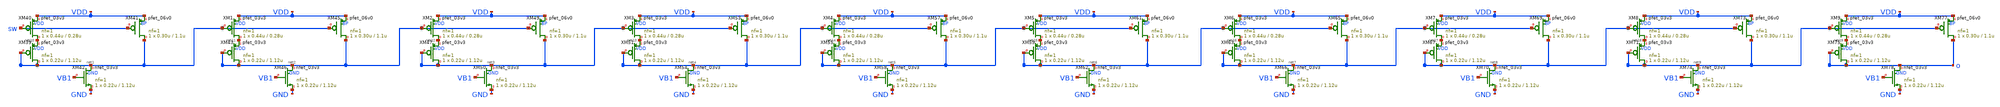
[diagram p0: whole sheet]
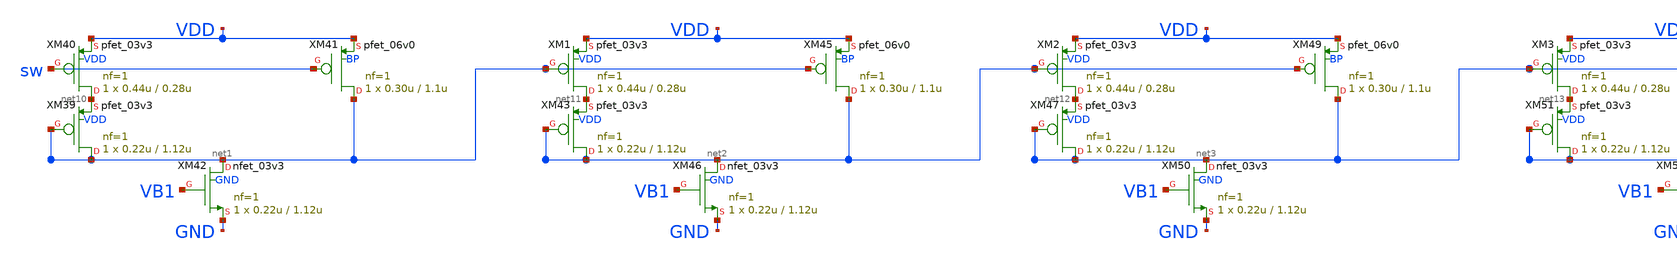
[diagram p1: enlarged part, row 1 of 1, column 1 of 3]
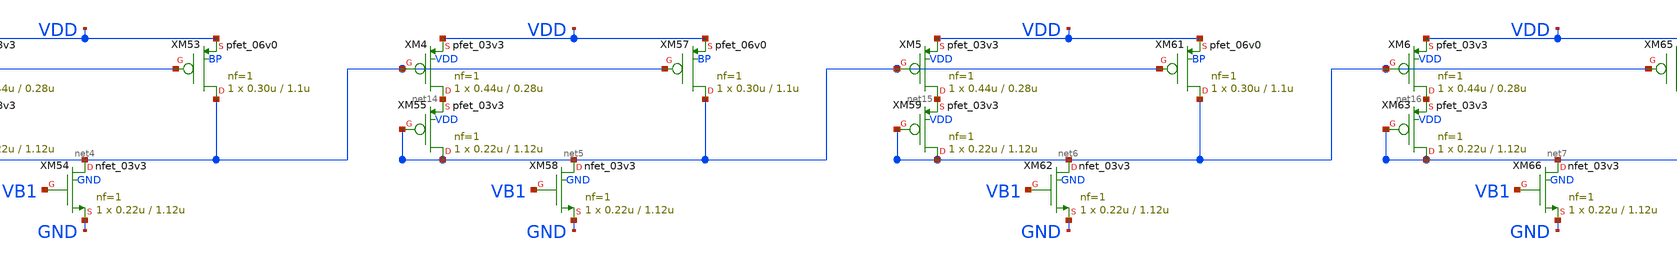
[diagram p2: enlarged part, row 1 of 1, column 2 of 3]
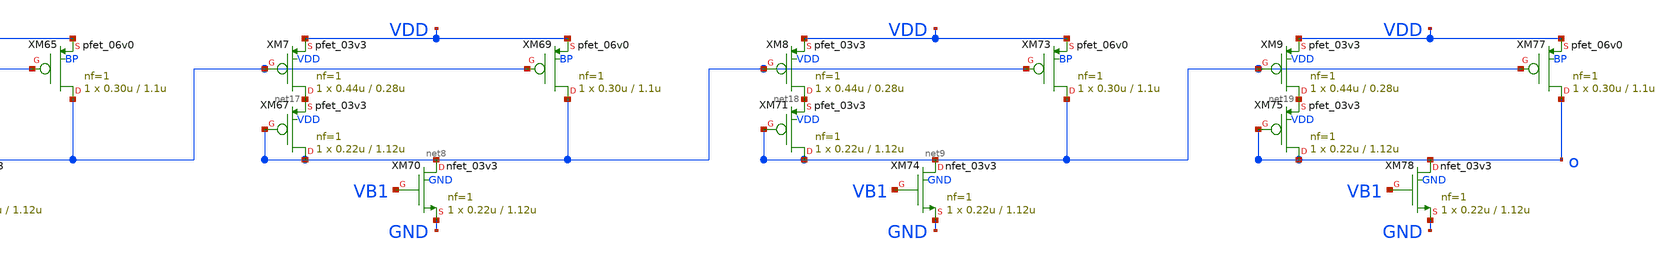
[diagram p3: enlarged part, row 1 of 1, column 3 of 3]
** sch_path: xschem_designs/STI_P_MC_TB.sch
**.subckt STI_P_MC_TB
XM39 net1 net1 net10 VDD pfet_03v3 L=1.12u W=0.22u nf=1 ad='int((nf+1)/2) * W/nf * 0.18u' as='int((nf+2)/2) * W/nf * 0.18u'
+ pd='2*int((nf+1)/2) * (W/nf + 0.18u)' ps='2*int((nf+2)/2) * (W/nf + 0.18u)' nrd='0.18u / W' nrs='0.18u / W'
+ sa=0 sb=0 sd=0 m=1 par=1
XM42 net1 VB1 GND GND nfet_03v3 L=1.12u W=0.22u nf=1 ad='int((nf+1)/2) * W/nf * 0.18u' as='int((nf+2)/2) * W/nf * 0.18u'
+ pd='2*int((nf+1)/2) * (W/nf + 0.18u)' ps='2*int((nf+2)/2) * (W/nf + 0.18u)' nrd='0.18u / W' nrs='0.18u / W'
+ sa=0 sb=0 sd=0 m=1 par=1
XM43 net2 net2 net11 VDD pfet_03v3 L=1.12u W=0.22u nf=1 ad='int((nf+1)/2) * W/nf * 0.18u' as='int((nf+2)/2) * W/nf * 0.18u'
+ pd='2*int((nf+1)/2) * (W/nf + 0.18u)' ps='2*int((nf+2)/2) * (W/nf + 0.18u)' nrd='0.18u / W' nrs='0.18u / W'
+ sa=0 sb=0 sd=0 m=1 par=1
XM46 net2 VB1 GND GND nfet_03v3 L=1.12u W=0.22u nf=1 ad='int((nf+1)/2) * W/nf * 0.18u' as='int((nf+2)/2) * W/nf * 0.18u'
+ pd='2*int((nf+1)/2) * (W/nf + 0.18u)' ps='2*int((nf+2)/2) * (W/nf + 0.18u)' nrd='0.18u / W' nrs='0.18u / W'
+ sa=0 sb=0 sd=0 m=1 par=1
XM47 net3 net3 net12 VDD pfet_03v3 L=1.12u W=0.22u nf=1 ad='int((nf+1)/2) * W/nf * 0.18u' as='int((nf+2)/2) * W/nf * 0.18u'
+ pd='2*int((nf+1)/2) * (W/nf + 0.18u)' ps='2*int((nf+2)/2) * (W/nf + 0.18u)' nrd='0.18u / W' nrs='0.18u / W'
+ sa=0 sb=0 sd=0 m=1 par=1
XM50 net3 VB1 GND GND nfet_03v3 L=1.12u W=0.22u nf=1 ad='int((nf+1)/2) * W/nf * 0.18u' as='int((nf+2)/2) * W/nf * 0.18u'
+ pd='2*int((nf+1)/2) * (W/nf + 0.18u)' ps='2*int((nf+2)/2) * (W/nf + 0.18u)' nrd='0.18u / W' nrs='0.18u / W'
+ sa=0 sb=0 sd=0 m=1 par=1
XM51 net4 net4 net13 VDD pfet_03v3 L=1.12u W=0.22u nf=1 ad='int((nf+1)/2) * W/nf * 0.18u' as='int((nf+2)/2) * W/nf * 0.18u'
+ pd='2*int((nf+1)/2) * (W/nf + 0.18u)' ps='2*int((nf+2)/2) * (W/nf + 0.18u)' nrd='0.18u / W' nrs='0.18u / W'
+ sa=0 sb=0 sd=0 m=1 par=1
XM54 net4 VB1 GND GND nfet_03v3 L=1.12u W=0.22u nf=1 ad='int((nf+1)/2) * W/nf * 0.18u' as='int((nf+2)/2) * W/nf * 0.18u'
+ pd='2*int((nf+1)/2) * (W/nf + 0.18u)' ps='2*int((nf+2)/2) * (W/nf + 0.18u)' nrd='0.18u / W' nrs='0.18u / W'
+ sa=0 sb=0 sd=0 m=1 par=1
XM55 net5 net5 net14 VDD pfet_03v3 L=1.12u W=0.22u nf=1 ad='int((nf+1)/2) * W/nf * 0.18u' as='int((nf+2)/2) * W/nf * 0.18u'
+ pd='2*int((nf+1)/2) * (W/nf + 0.18u)' ps='2*int((nf+2)/2) * (W/nf + 0.18u)' nrd='0.18u / W' nrs='0.18u / W'
+ sa=0 sb=0 sd=0 m=1 par=1
XM58 net5 VB1 GND GND nfet_03v3 L=1.12u W=0.22u nf=1 ad='int((nf+1)/2) * W/nf * 0.18u' as='int((nf+2)/2) * W/nf * 0.18u'
+ pd='2*int((nf+1)/2) * (W/nf + 0.18u)' ps='2*int((nf+2)/2) * (W/nf + 0.18u)' nrd='0.18u / W' nrs='0.18u / W'
+ sa=0 sb=0 sd=0 m=1 par=1
XM59 net6 net6 net15 VDD pfet_03v3 L=1.12u W=0.22u nf=1 ad='int((nf+1)/2) * W/nf * 0.18u' as='int((nf+2)/2) * W/nf * 0.18u'
+ pd='2*int((nf+1)/2) * (W/nf + 0.18u)' ps='2*int((nf+2)/2) * (W/nf + 0.18u)' nrd='0.18u / W' nrs='0.18u / W'
+ sa=0 sb=0 sd=0 m=1 par=1
XM62 net6 VB1 GND GND nfet_03v3 L=1.12u W=0.22u nf=1 ad='int((nf+1)/2) * W/nf * 0.18u' as='int((nf+2)/2) * W/nf * 0.18u'
+ pd='2*int((nf+1)/2) * (W/nf + 0.18u)' ps='2*int((nf+2)/2) * (W/nf + 0.18u)' nrd='0.18u / W' nrs='0.18u / W'
+ sa=0 sb=0 sd=0 m=1 par=1
XM63 net7 net7 net16 VDD pfet_03v3 L=1.12u W=0.22u nf=1 ad='int((nf+1)/2) * W/nf * 0.18u' as='int((nf+2)/2) * W/nf * 0.18u'
+ pd='2*int((nf+1)/2) * (W/nf + 0.18u)' ps='2*int((nf+2)/2) * (W/nf + 0.18u)' nrd='0.18u / W' nrs='0.18u / W'
+ sa=0 sb=0 sd=0 m=1 par=1
XM66 net7 VB1 GND GND nfet_03v3 L=1.12u W=0.22u nf=1 ad='int((nf+1)/2) * W/nf * 0.18u' as='int((nf+2)/2) * W/nf * 0.18u'
+ pd='2*int((nf+1)/2) * (W/nf + 0.18u)' ps='2*int((nf+2)/2) * (W/nf + 0.18u)' nrd='0.18u / W' nrs='0.18u / W'
+ sa=0 sb=0 sd=0 m=1 par=1
XM67 net8 net8 net17 VDD pfet_03v3 L=1.12u W=0.22u nf=1 ad='int((nf+1)/2) * W/nf * 0.18u' as='int((nf+2)/2) * W/nf * 0.18u'
+ pd='2*int((nf+1)/2) * (W/nf + 0.18u)' ps='2*int((nf+2)/2) * (W/nf + 0.18u)' nrd='0.18u / W' nrs='0.18u / W'
+ sa=0 sb=0 sd=0 m=1 par=1
XM70 net8 VB1 GND GND nfet_03v3 L=1.12u W=0.22u nf=1 ad='int((nf+1)/2) * W/nf * 0.18u' as='int((nf+2)/2) * W/nf * 0.18u'
+ pd='2*int((nf+1)/2) * (W/nf + 0.18u)' ps='2*int((nf+2)/2) * (W/nf + 0.18u)' nrd='0.18u / W' nrs='0.18u / W'
+ sa=0 sb=0 sd=0 m=1 par=1
XM71 net9 net9 net18 VDD pfet_03v3 L=1.12u W=0.22u nf=1 ad='int((nf+1)/2) * W/nf * 0.18u' as='int((nf+2)/2) * W/nf * 0.18u'
+ pd='2*int((nf+1)/2) * (W/nf + 0.18u)' ps='2*int((nf+2)/2) * (W/nf + 0.18u)' nrd='0.18u / W' nrs='0.18u / W'
+ sa=0 sb=0 sd=0 m=1 par=1
XM74 net9 VB1 GND GND nfet_03v3 L=1.12u W=0.22u nf=1 ad='int((nf+1)/2) * W/nf * 0.18u' as='int((nf+2)/2) * W/nf * 0.18u'
+ pd='2*int((nf+1)/2) * (W/nf + 0.18u)' ps='2*int((nf+2)/2) * (W/nf + 0.18u)' nrd='0.18u / W' nrs='0.18u / W'
+ sa=0 sb=0 sd=0 m=1 par=1
XM75 o o net19 VDD pfet_03v3 L=1.12u W=0.22u nf=1 ad='int((nf+1)/2) * W/nf * 0.18u' as='int((nf+2)/2) * W/nf * 0.18u'
+ pd='2*int((nf+1)/2) * (W/nf + 0.18u)' ps='2*int((nf+2)/2) * (W/nf + 0.18u)' nrd='0.18u / W' nrs='0.18u / W'
+ sa=0 sb=0 sd=0 m=1 par=1
XM78 o VB1 GND GND nfet_03v3 L=1.12u W=0.22u nf=1 ad='int((nf+1)/2) * W/nf * 0.18u' as='int((nf+2)/2) * W/nf * 0.18u'
+ pd='2*int((nf+1)/2) * (W/nf + 0.18u)' ps='2*int((nf+2)/2) * (W/nf + 0.18u)' nrd='0.18u / W' nrs='0.18u / W'
+ sa=0 sb=0 sd=0 m=1 par=1
XM41 net1 sw VDD BP pfet_06v0 L=1.1u W=0.30u nf=1 ad='int((nf+1)/2) * W/nf * 0.18u' as='int((nf+2)/2) * W/nf * 0.18u'
+ pd='2*int((nf+1)/2) * (W/nf + 0.18u)' ps='2*int((nf+2)/2) * (W/nf + 0.18u)' nrd='0.18u / W' nrs='0.18u / W'
+ sa=0 sb=0 sd=0 m=1 par=1
XM45 net2 net1 VDD BP pfet_06v0 L=1.1u W=0.30u nf=1 ad='int((nf+1)/2) * W/nf * 0.18u' as='int((nf+2)/2) * W/nf * 0.18u'
+ pd='2*int((nf+1)/2) * (W/nf + 0.18u)' ps='2*int((nf+2)/2) * (W/nf + 0.18u)' nrd='0.18u / W' nrs='0.18u / W'
+ sa=0 sb=0 sd=0 m=1 par=1
XM49 net3 net2 VDD BP pfet_06v0 L=1.1u W=0.30u nf=1 ad='int((nf+1)/2) * W/nf * 0.18u' as='int((nf+2)/2) * W/nf * 0.18u'
+ pd='2*int((nf+1)/2) * (W/nf + 0.18u)' ps='2*int((nf+2)/2) * (W/nf + 0.18u)' nrd='0.18u / W' nrs='0.18u / W'
+ sa=0 sb=0 sd=0 m=1 par=1
XM53 net4 net3 VDD BP pfet_06v0 L=1.1u W=0.30u nf=1 ad='int((nf+1)/2) * W/nf * 0.18u' as='int((nf+2)/2) * W/nf * 0.18u'
+ pd='2*int((nf+1)/2) * (W/nf + 0.18u)' ps='2*int((nf+2)/2) * (W/nf + 0.18u)' nrd='0.18u / W' nrs='0.18u / W'
+ sa=0 sb=0 sd=0 m=1 par=1
XM57 net5 net4 VDD BP pfet_06v0 L=1.1u W=0.30u nf=1 ad='int((nf+1)/2) * W/nf * 0.18u' as='int((nf+2)/2) * W/nf * 0.18u'
+ pd='2*int((nf+1)/2) * (W/nf + 0.18u)' ps='2*int((nf+2)/2) * (W/nf + 0.18u)' nrd='0.18u / W' nrs='0.18u / W'
+ sa=0 sb=0 sd=0 m=1 par=1
XM61 net6 net5 VDD BP pfet_06v0 L=1.1u W=0.30u nf=1 ad='int((nf+1)/2) * W/nf * 0.18u' as='int((nf+2)/2) * W/nf * 0.18u'
+ pd='2*int((nf+1)/2) * (W/nf + 0.18u)' ps='2*int((nf+2)/2) * (W/nf + 0.18u)' nrd='0.18u / W' nrs='0.18u / W'
+ sa=0 sb=0 sd=0 m=1 par=1
XM65 net7 net6 VDD BP pfet_06v0 L=1.1u W=0.30u nf=1 ad='int((nf+1)/2) * W/nf * 0.18u' as='int((nf+2)/2) * W/nf * 0.18u'
+ pd='2*int((nf+1)/2) * (W/nf + 0.18u)' ps='2*int((nf+2)/2) * (W/nf + 0.18u)' nrd='0.18u / W' nrs='0.18u / W'
+ sa=0 sb=0 sd=0 m=1 par=1
XM69 net8 net7 VDD BP pfet_06v0 L=1.1u W=0.30u nf=1 ad='int((nf+1)/2) * W/nf * 0.18u' as='int((nf+2)/2) * W/nf * 0.18u'
+ pd='2*int((nf+1)/2) * (W/nf + 0.18u)' ps='2*int((nf+2)/2) * (W/nf + 0.18u)' nrd='0.18u / W' nrs='0.18u / W'
+ sa=0 sb=0 sd=0 m=1 par=1
XM73 net9 net8 VDD BP pfet_06v0 L=1.1u W=0.30u nf=1 ad='int((nf+1)/2) * W/nf * 0.18u' as='int((nf+2)/2) * W/nf * 0.18u'
+ pd='2*int((nf+1)/2) * (W/nf + 0.18u)' ps='2*int((nf+2)/2) * (W/nf + 0.18u)' nrd='0.18u / W' nrs='0.18u / W'
+ sa=0 sb=0 sd=0 m=1 par=1
XM77 o net9 VDD BP pfet_06v0 L=1.1u W=0.30u nf=1 ad='int((nf+1)/2) * W/nf * 0.18u' as='int((nf+2)/2) * W/nf * 0.18u'
+ pd='2*int((nf+1)/2) * (W/nf + 0.18u)' ps='2*int((nf+2)/2) * (W/nf + 0.18u)' nrd='0.18u / W' nrs='0.18u / W'
+ sa=0 sb=0 sd=0 m=1 par=1
XM40 net10 sw VDD VDD pfet_03v3 L=0.28u W=0.44u nf=1 ad='int((nf+1)/2) * W/nf * 0.18u' as='int((nf+2)/2) * W/nf * 0.18u'
+ pd='2*int((nf+1)/2) * (W/nf + 0.18u)' ps='2*int((nf+2)/2) * (W/nf + 0.18u)' nrd='0.18u / W' nrs='0.18u / W'
+ sa=0 sb=0 sd=0 m=1 par=1
XM1 net11 net1 VDD VDD pfet_03v3 L=0.28u W=0.44u nf=1 ad='int((nf+1)/2) * W/nf * 0.18u' as='int((nf+2)/2) * W/nf * 0.18u'
+ pd='2*int((nf+1)/2) * (W/nf + 0.18u)' ps='2*int((nf+2)/2) * (W/nf + 0.18u)' nrd='0.18u / W' nrs='0.18u / W'
+ sa=0 sb=0 sd=0 m=1 par=1
XM2 net12 net2 VDD VDD pfet_03v3 L=0.28u W=0.44u nf=1 ad='int((nf+1)/2) * W/nf * 0.18u' as='int((nf+2)/2) * W/nf * 0.18u'
+ pd='2*int((nf+1)/2) * (W/nf + 0.18u)' ps='2*int((nf+2)/2) * (W/nf + 0.18u)' nrd='0.18u / W' nrs='0.18u / W'
+ sa=0 sb=0 sd=0 m=1 par=1
XM3 net13 net3 VDD VDD pfet_03v3 L=0.28u W=0.44u nf=1 ad='int((nf+1)/2) * W/nf * 0.18u' as='int((nf+2)/2) * W/nf * 0.18u'
+ pd='2*int((nf+1)/2) * (W/nf + 0.18u)' ps='2*int((nf+2)/2) * (W/nf + 0.18u)' nrd='0.18u / W' nrs='0.18u / W'
+ sa=0 sb=0 sd=0 m=1 par=1
XM4 net14 net4 VDD VDD pfet_03v3 L=0.28u W=0.44u nf=1 ad='int((nf+1)/2) * W/nf * 0.18u' as='int((nf+2)/2) * W/nf * 0.18u'
+ pd='2*int((nf+1)/2) * (W/nf + 0.18u)' ps='2*int((nf+2)/2) * (W/nf + 0.18u)' nrd='0.18u / W' nrs='0.18u / W'
+ sa=0 sb=0 sd=0 m=1 par=1
XM5 net15 net5 VDD VDD pfet_03v3 L=0.28u W=0.44u nf=1 ad='int((nf+1)/2) * W/nf * 0.18u' as='int((nf+2)/2) * W/nf * 0.18u'
+ pd='2*int((nf+1)/2) * (W/nf + 0.18u)' ps='2*int((nf+2)/2) * (W/nf + 0.18u)' nrd='0.18u / W' nrs='0.18u / W'
+ sa=0 sb=0 sd=0 m=1 par=1
XM6 net16 net6 VDD VDD pfet_03v3 L=0.28u W=0.44u nf=1 ad='int((nf+1)/2) * W/nf * 0.18u' as='int((nf+2)/2) * W/nf * 0.18u'
+ pd='2*int((nf+1)/2) * (W/nf + 0.18u)' ps='2*int((nf+2)/2) * (W/nf + 0.18u)' nrd='0.18u / W' nrs='0.18u / W'
+ sa=0 sb=0 sd=0 m=1 par=1
XM7 net17 net7 VDD VDD pfet_03v3 L=0.28u W=0.44u nf=1 ad='int((nf+1)/2) * W/nf * 0.18u' as='int((nf+2)/2) * W/nf * 0.18u'
+ pd='2*int((nf+1)/2) * (W/nf + 0.18u)' ps='2*int((nf+2)/2) * (W/nf + 0.18u)' nrd='0.18u / W' nrs='0.18u / W'
+ sa=0 sb=0 sd=0 m=1 par=1
XM8 net18 net8 VDD VDD pfet_03v3 L=0.28u W=0.44u nf=1 ad='int((nf+1)/2) * W/nf * 0.18u' as='int((nf+2)/2) * W/nf * 0.18u'
+ pd='2*int((nf+1)/2) * (W/nf + 0.18u)' ps='2*int((nf+2)/2) * (W/nf + 0.18u)' nrd='0.18u / W' nrs='0.18u / W'
+ sa=0 sb=0 sd=0 m=1 par=1
XM9 net19 net9 VDD VDD pfet_03v3 L=0.28u W=0.44u nf=1 ad='int((nf+1)/2) * W/nf * 0.18u' as='int((nf+2)/2) * W/nf * 0.18u'
+ pd='2*int((nf+1)/2) * (W/nf + 0.18u)' ps='2*int((nf+2)/2) * (W/nf + 0.18u)' nrd='0.18u / W' nrs='0.18u / W'
+ sa=0 sb=0 sd=0 m=1 par=1
**** begin user architecture code


.global VDD GND BP BN
.option temp=15
.include /usr/local/share/pdk/gf180mcuC/libs.tech/ngspice/design.ngspice
.lib /usr/local/share/pdk/gf180mcuC/libs.tech/ngspice/sm141064.ngspice statistical

Vdd VDD 0 3.3
Vbp BP VDD 2.7
Vb VB1 GND 1
Vin sw 0 DC 0

.param sw_stat_global = 1
.param sw_stat_mismatch = 1

.control
  let runs = 500
  let run = 1

  option seed = 12345

  dowhile run <= runs
    dc Vin 0 3.3 0.001
    linearize
    wrdata MC/STI_stat/STI_P_TB_MC3_t15{$&run}.txt v(o)
    reset
    let run = run + 1
  end
.endc


**** end user architecture code
**.ends
.end
